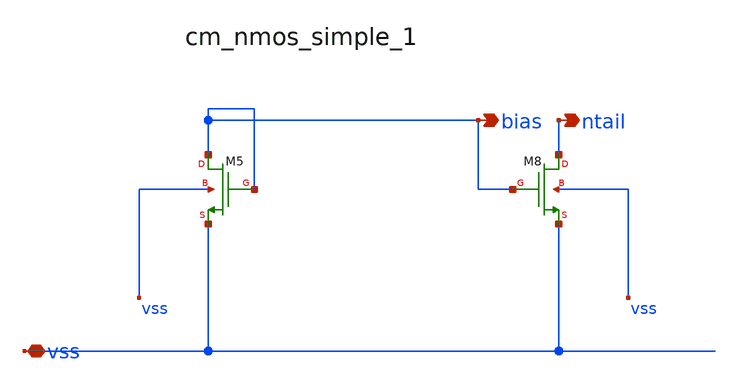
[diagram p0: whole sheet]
** sch_path: analog-db/raw/cmfb_003_5t_nmos_input/hier/blocks/cm_nmos_simple_1.sch
**.subckt cm_nmos_simple_1 vss bias ntail
*.iopin vss
*.opin bias
*.opin ntail
XM5 bias bias vss vss sg13_lv_nmos w=x_dut_xm5_w l=x_dut_xm5_l ng=1 m=x_dut_xm5_m
XM8 ntail bias vss vss sg13_lv_nmos w=x_dut_xm8_w l=x_dut_xm8_l ng=1 m=x_dut_xm8_m
**.ends
.end
